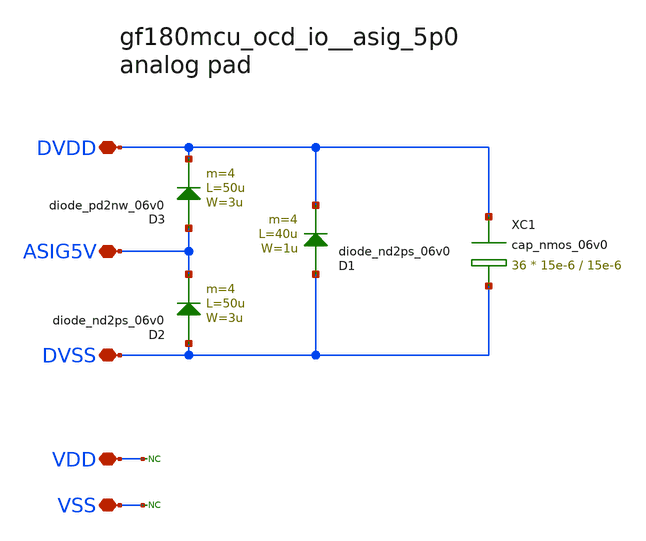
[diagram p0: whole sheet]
** sch_path: cells/asig_5p0/gf180mcu_ocd_io__asig_5p0.sch
**.subckt gf180mcu_ocd_io__asig_5p0 DVDD DVSS VDD VSS ASIG5V
*.iopin DVDD
*.iopin DVSS
*.iopin VDD
*.iopin VSS
*.iopin ASIG5V
D1 DVSS DVDD diode_nd2ps_06v0 area='1u * 40u ' pj='2*1u + 2*40u ' m=4
D2 DVSS ASIG5V diode_nd2ps_06v0 area='3u * 50u ' pj='2*3u + 2*50u ' m=4
D3 ASIG5V DVDD diode_pd2nw_06v0 area='3u * 50u ' pj='2*3u + 2*50u ' m=4
XC1 DVDD DVSS cap_nmos_06v0 c_width=15e-6 c_length=15e-6 m=36
* noconn VDD
* noconn VSS
**.ends
.end
